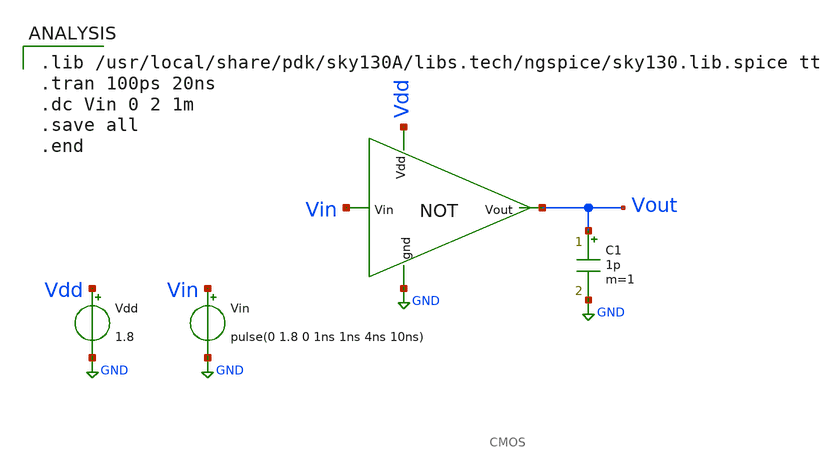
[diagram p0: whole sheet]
** sch_path: Design-and-analysis-of-CMOS-ineverter/XSCHEM FILES/CMOS_test.sch
**.subckt CMOS_test
x1 Vdd Vout GND Vin CMOS
Vdd Vdd GND 1.8
Vin Vin GND pulse(0 1.8 0 1ns 1ns 4ns 10ns)
C1 Vout GND 1p m=1
**** begin user architecture code

.lib /usr/local/share/pdk/sky130A/libs.tech/ngspice/sky130.lib.spice tt
.tran 100ps 20ns
.dc Vin 0 2 1m
.save all
.end

**** end user architecture code
**.ends

* expanding   symbol:  CMOS.sym # of pins=4
** sym_path: Design-and-analysis-of-CMOS-ineverter/XSCHEM FILES/CMOS.sym
** sch_path: Design-and-analysis-of-CMOS-ineverter/XSCHEM FILES/CMOS.sch
.subckt CMOS Vdd Vout gnd Vin
*.ipin Vin
*.ipin Vdd
*.ipin gnd
*.opin Vout
XM1 Vout Vin Vdd Vdd sky130_fd_pr__pfet_01v8 L=0.15 W=2.5 nf=1 ad='int((nf+1)/2) * W/nf * 0.29' as='int((nf+2)/2) * W/nf * 0.29'
+ pd='2*int((nf+1)/2) * (W/nf + 0.29)' ps='2*int((nf+2)/2) * (W/nf + 0.29)' nrd='0.29 / W' nrs='0.29 / W'
+ sa=0 sb=0 sd=0 mult=1 m=1
XM2 Vout Vin gnd gnd sky130_fd_pr__nfet_01v8 L=0.15 W=1 nf=1 ad='int((nf+1)/2) * W/nf * 0.29' as='int((nf+2)/2) * W/nf * 0.29'
+ pd='2*int((nf+1)/2) * (W/nf + 0.29)' ps='2*int((nf+2)/2) * (W/nf + 0.29)' nrd='0.29 / W' nrs='0.29 / W'
+ sa=0 sb=0 sd=0 mult=1 m=1
.ends

.GLOBAL GND
.end
